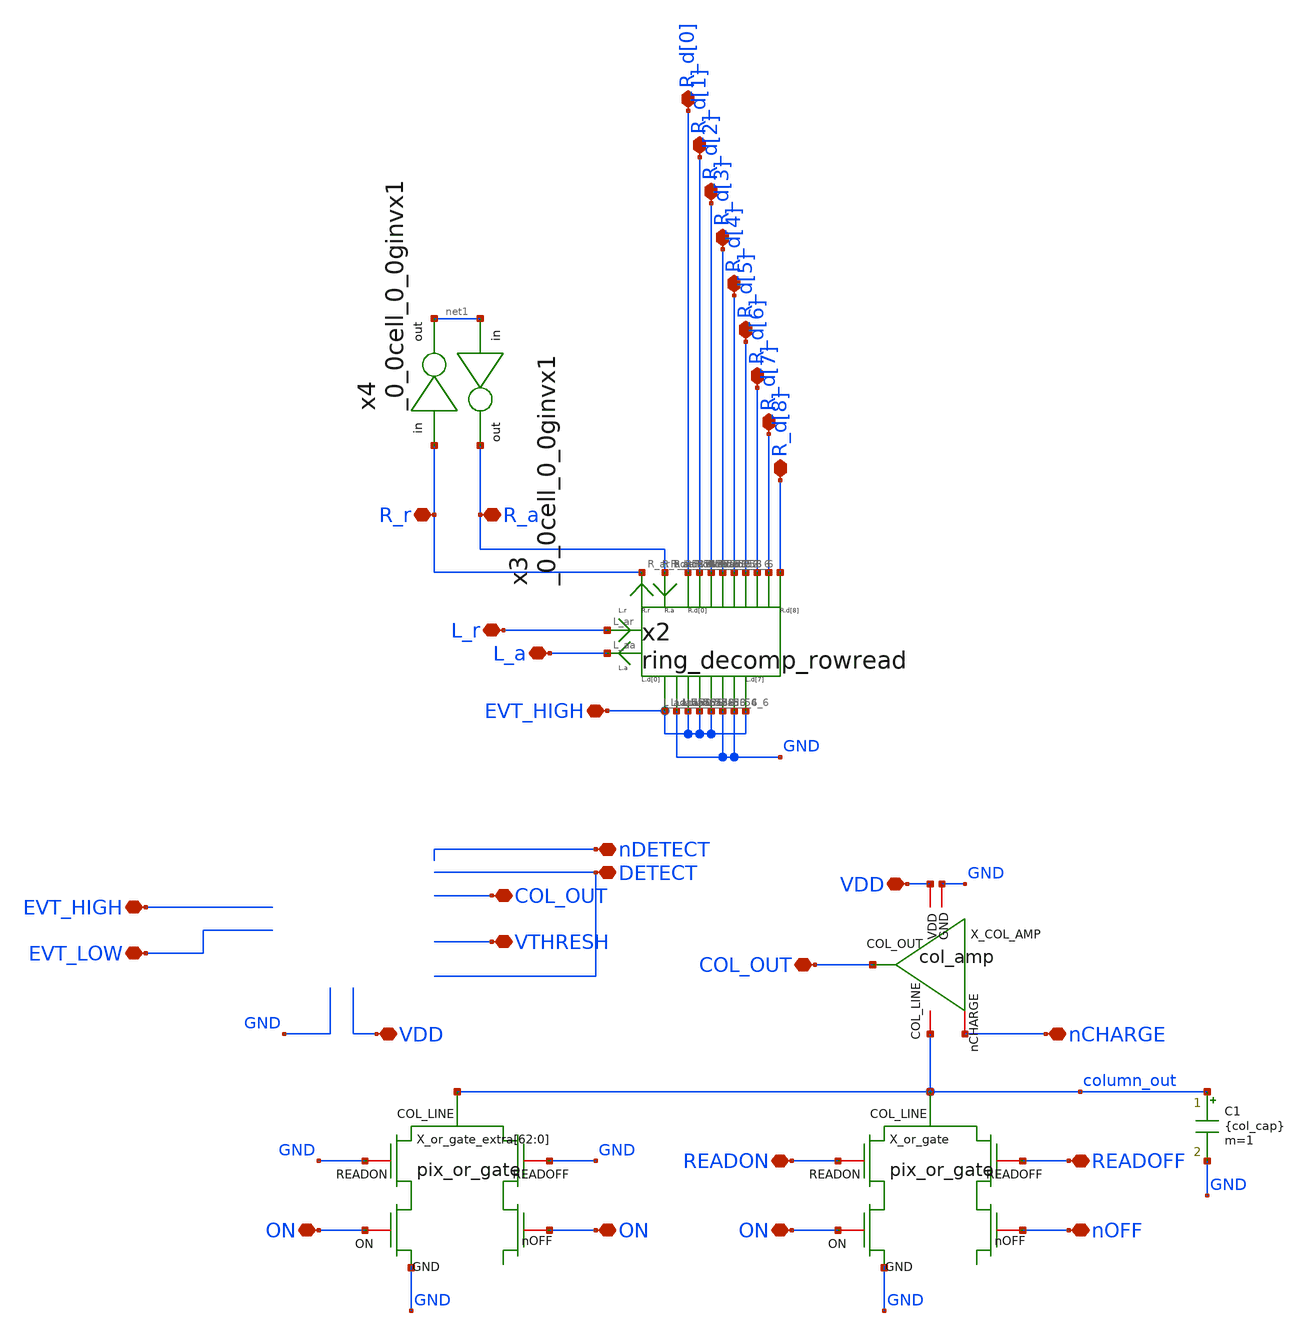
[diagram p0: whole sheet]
** sch_path: analog/xschem/col_amp_v2_std_vds/xschem/TRAN_TB_ASYNC.sch
**.subckt TRAN_TB_ASYNC nCHARGE nOFF READOFF ON READON VDD COL_OUT ON ON DETECT VTHRESH VDD EVT_HIGH
*+ EVT_LOW EVT_HIGH nDETECT L_r L_a R_d[0] R_d[1] R_d[2] R_d[3] R_d[4] R_d[5] R_d[6] R_d[7] R_d[8] R_r R_a
*+ COL_OUT
*.iopin nCHARGE
*.iopin nOFF
*.iopin READOFF
*.iopin ON
*.iopin READON
*.iopin VDD
*.iopin COL_OUT
*.iopin ON
*.iopin ON
*.iopin DETECT
*.iopin VTHRESH
*.iopin VDD
*.iopin EVT_HIGH
*.iopin EVT_LOW
*.iopin EVT_HIGH
*.iopin nDETECT
*.iopin L_r
*.iopin L_a
*.iopin R_d[0]
*.iopin R_d[1]
*.iopin R_d[2]
*.iopin R_d[3]
*.iopin R_d[4]
*.iopin R_d[5]
*.iopin R_d[6]
*.iopin R_d[7]
*.iopin R_d[8]
*.iopin R_r
*.iopin R_a
*.iopin COL_OUT
X_COL_AMP VDD nCHARGE COL_OUT GND column_out col_amp
C1 column_out GND {col_cap} m=1
X_or_gate column_out READOFF READON nOFF ON GND pix_or_gate
X_or_gate_extra[62] column_out GND GND ON ON GND pix_or_gate
X_or_gate_extra[61] column_out GND GND ON ON GND pix_or_gate
X_or_gate_extra[60] column_out GND GND ON ON GND pix_or_gate
X_or_gate_extra[59] column_out GND GND ON ON GND pix_or_gate
X_or_gate_extra[58] column_out GND GND ON ON GND pix_or_gate
X_or_gate_extra[57] column_out GND GND ON ON GND pix_or_gate
X_or_gate_extra[56] column_out GND GND ON ON GND pix_or_gate
X_or_gate_extra[55] column_out GND GND ON ON GND pix_or_gate
X_or_gate_extra[54] column_out GND GND ON ON GND pix_or_gate
X_or_gate_extra[53] column_out GND GND ON ON GND pix_or_gate
X_or_gate_extra[52] column_out GND GND ON ON GND pix_or_gate
X_or_gate_extra[51] column_out GND GND ON ON GND pix_or_gate
X_or_gate_extra[50] column_out GND GND ON ON GND pix_or_gate
X_or_gate_extra[49] column_out GND GND ON ON GND pix_or_gate
X_or_gate_extra[48] column_out GND GND ON ON GND pix_or_gate
X_or_gate_extra[47] column_out GND GND ON ON GND pix_or_gate
X_or_gate_extra[46] column_out GND GND ON ON GND pix_or_gate
X_or_gate_extra[45] column_out GND GND ON ON GND pix_or_gate
X_or_gate_extra[44] column_out GND GND ON ON GND pix_or_gate
X_or_gate_extra[43] column_out GND GND ON ON GND pix_or_gate
X_or_gate_extra[42] column_out GND GND ON ON GND pix_or_gate
X_or_gate_extra[41] column_out GND GND ON ON GND pix_or_gate
X_or_gate_extra[40] column_out GND GND ON ON GND pix_or_gate
X_or_gate_extra[39] column_out GND GND ON ON GND pix_or_gate
X_or_gate_extra[38] column_out GND GND ON ON GND pix_or_gate
X_or_gate_extra[37] column_out GND GND ON ON GND pix_or_gate
X_or_gate_extra[36] column_out GND GND ON ON GND pix_or_gate
X_or_gate_extra[35] column_out GND GND ON ON GND pix_or_gate
X_or_gate_extra[34] column_out GND GND ON ON GND pix_or_gate
X_or_gate_extra[33] column_out GND GND ON ON GND pix_or_gate
X_or_gate_extra[32] column_out GND GND ON ON GND pix_or_gate
X_or_gate_extra[31] column_out GND GND ON ON GND pix_or_gate
X_or_gate_extra[30] column_out GND GND ON ON GND pix_or_gate
X_or_gate_extra[29] column_out GND GND ON ON GND pix_or_gate
X_or_gate_extra[28] column_out GND GND ON ON GND pix_or_gate
X_or_gate_extra[27] column_out GND GND ON ON GND pix_or_gate
X_or_gate_extra[26] column_out GND GND ON ON GND pix_or_gate
X_or_gate_extra[25] column_out GND GND ON ON GND pix_or_gate
X_or_gate_extra[24] column_out GND GND ON ON GND pix_or_gate
X_or_gate_extra[23] column_out GND GND ON ON GND pix_or_gate
X_or_gate_extra[22] column_out GND GND ON ON GND pix_or_gate
X_or_gate_extra[21] column_out GND GND ON ON GND pix_or_gate
X_or_gate_extra[20] column_out GND GND ON ON GND pix_or_gate
X_or_gate_extra[19] column_out GND GND ON ON GND pix_or_gate
X_or_gate_extra[18] column_out GND GND ON ON GND pix_or_gate
X_or_gate_extra[17] column_out GND GND ON ON GND pix_or_gate
X_or_gate_extra[16] column_out GND GND ON ON GND pix_or_gate
X_or_gate_extra[15] column_out GND GND ON ON GND pix_or_gate
X_or_gate_extra[14] column_out GND GND ON ON GND pix_or_gate
X_or_gate_extra[13] column_out GND GND ON ON GND pix_or_gate
X_or_gate_extra[12] column_out GND GND ON ON GND pix_or_gate
X_or_gate_extra[11] column_out GND GND ON ON GND pix_or_gate
X_or_gate_extra[10] column_out GND GND ON ON GND pix_or_gate
X_or_gate_extra[9] column_out GND GND ON ON GND pix_or_gate
X_or_gate_extra[8] column_out GND GND ON ON GND pix_or_gate
X_or_gate_extra[7] column_out GND GND ON ON GND pix_or_gate
X_or_gate_extra[6] column_out GND GND ON ON GND pix_or_gate
X_or_gate_extra[5] column_out GND GND ON ON GND pix_or_gate
X_or_gate_extra[4] column_out GND GND ON ON GND pix_or_gate
X_or_gate_extra[3] column_out GND GND ON ON GND pix_or_gate
X_or_gate_extra[2] column_out GND GND ON ON GND pix_or_gate
X_or_gate_extra[1] column_out GND GND ON ON GND pix_or_gate
X_or_gate_extra[0] column_out GND GND ON ON GND pix_or_gate
x3 net1 R_a _0_0cell_0_0ginvx1
x4 R_r net1 _0_0cell_0_0ginvx1
x2 EVT_HIGH GND EVT_HIGH EVT_HIGH EVT_HIGH GND GND EVT_HIGH L_r L_a R_d[0] R_d[1] R_d[2] R_d[3]
+ R_d[4] R_d[5] R_d[6] R_d[7] R_d[8] R_r R_a ring_decomp_rowread
**** begin user architecture code


.lib /home/alienfalcon/.ciel/sky130B/libs.tech/combined/sky130.lib.spice tt
.include /home/alienfalcon/Projects/skywater/open_dvs_py312/open_dvs/dvs_2026/col_amp/xschem/read_row8.sp

.option rshunt=1000T
.option trtol=7 abstol=1p chgtol=4e-16 vntol=1e-6 reltol=1e-4
.option temp=27

.GLOBAL VDD
.GLOBAL GND
.GLOBAL Reset

.param vdd = 1.8 	//supply voltage
.param tr = 1p		//rise time of voltage source signals
.param tf = 1p		//fall time of voltage source signals
.param pw = 30n		//pulse width
.param pw_chrg = 30n	//pulse width for ncharge signal
.param pw_rd = 380n	//pulse width for read signal
.param pw_det = 60n
.param pw_del = 30n	//setup and hold delays for pulses
.param pw_ld = 20n	//hold delay for latch for async
.param thresh = 1.05	//threshold voltage for comparator
.param col_cap = 300f	//column line capacitance

.param read_time = {2*pw_chrg + 2*pw_rd + 6*pw_del}

V_VDD VDD GND DC {vdd}
V_ON ON GND DC {vdd-0.2}
V_nOFF nOFF GND DC 0.2
V_THRESH VTHRESH GND DC {thresh}
E_nDETECT nDETECT VDD DETECT GND -1
E_RESET Reset VDD nCHARGE GND -1

V_READON READOFF GND pulse(0 {vdd} {2*pw_chrg + 4*pw_del + pw_rd} {tr} {tf} {pw_det+pw_del} {read_time})
V_READOFF READON GND pulse(0 {vdd} {pw_chrg + pw_del} {tr} {tf} {pw_det+pw_del} {read_time})

V_nCHARGE nCHARGE GND pulse({vdd} 0 0 {tr} {tf} {pw_chrg} {read_time/2})
V_DETECT DETECT GND pulse(0 {vdd} {pw_chrg + 2*pw_del} {tr} {tf} {pw_det} {read_time/2})
V_LATCH L_r GND pulse(0 {vdd} {pw_chrg+ 2*pw_del + pw_ld} {tr} {tf} {pw_det-pw_ld} {read_time/2})


.control
	save v(column_out) v(nCHARGE) v(COL_OUT) v(ON) v(nOFF) v(READON) v(READOFF) v(DETECT)
	save v(EVT_HIGH) v(EVT_LOW) v(VTHRESH)
	save v(L_a) v(L_r) v(R_r) v(R_a) v(Reset)
	save v(R_d[0]) v(R_d[1]) v(R_d[2]) v(R_d[3]) v(R_d[4]) v(R_d[5]) v(R_d[6]) v(R_d[7]) v(R_d[8])
	save nosub nointernals

	tran 1n 2u uic
	let Vc_max = 0
	let Vc_min = 0
	let tr_col_out = 0
	let tf_col_out = 0
	let tset_col_low = 0
	let tset_col_high = 0

	*meas tran Vc_max FIND v(COL_OUT) AT=1.3u
	*meas tran Vc_min FIND v(COL_OUT) AT=0.3u

	*let V_diff = Vc_max - Vc_min
	*let Vc_10 = V_diff*0.1 + Vc_min
	*let Vc_90 = V_diff*0.9 + Vc_min
	*let Vc_set_low = Vc_max*0.98
	*let Vc_set_high = Vc_max*1.02

	*meas tran tr_col_out TRIG v(COL_OUT) VAL=Vc_10 CROSS=1 TARG v(COL_OUT) VAL=Vc_90 CROSS=1
	*meas tran tf_col_out TRIG v(COL_OUT) VAL=Vc_90 CROSS=2 TARG v(COL_OUT) VAL=Vc_10 CROSS=2
	*meas tran tset_col_low WHEN v(COL_OUT)=Vc_set_low RISE=LAST
	*meas tran tset_col_high WHEN v(COL_OUT)=Vc_set_high FALL=LAST

	*print Vc_max Vc_min
	*print tr_col_out tf_col_out tset_col_low tset_col_high

	*save tr_col_out tf_col_out tset_col_low tset_col_high

	write TRAN_TB_ASYNC.raw
.endc




**** end user architecture code
**.ends
.end
